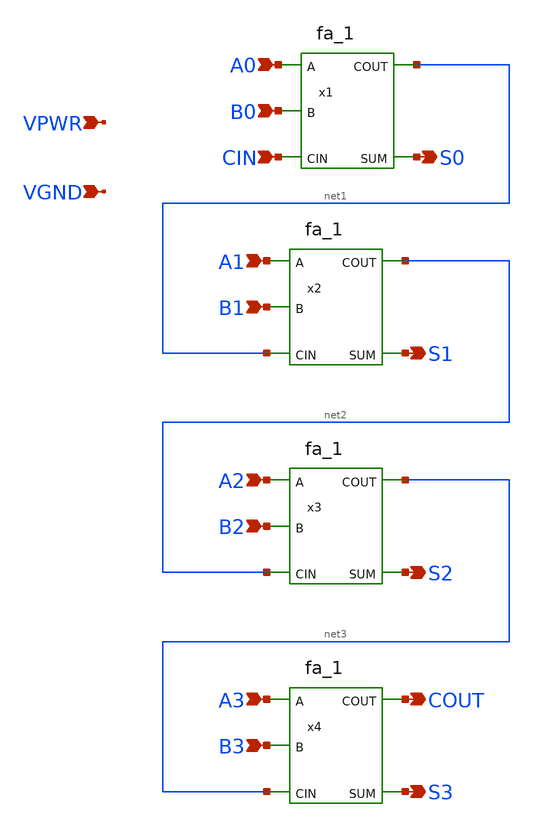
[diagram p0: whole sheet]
** sch_path: xschem/full_adder_4bit.sch
**.subckt full_adder_4bit A0 B0 A1 B1 A2 B2 A3 B3 S0 S1 S2 S3 COUT CIN VPWR VGND
*.ipin A0
*.ipin B0
*.ipin A1
*.ipin B1
*.ipin A2
*.ipin B2
*.ipin A3
*.ipin B3
*.opin S0
*.opin S1
*.opin S2
*.opin S3
*.opin COUT
*.ipin CIN
*.ipin VPWR
*.ipin VGND
x1 A0 B0 CIN VGND VGND VPWR VPWR net1 S0 sky130_fd_sc_hd__fa_1
x2 A1 B1 net1 VGND VGND VPWR VPWR net2 S1 sky130_fd_sc_hd__fa_1
x3 A2 B2 net2 VGND VGND VPWR VPWR net3 S2 sky130_fd_sc_hd__fa_1
x4 A3 B3 net3 VGND VGND VPWR VPWR COUT S3 sky130_fd_sc_hd__fa_1
**.ends
.end
